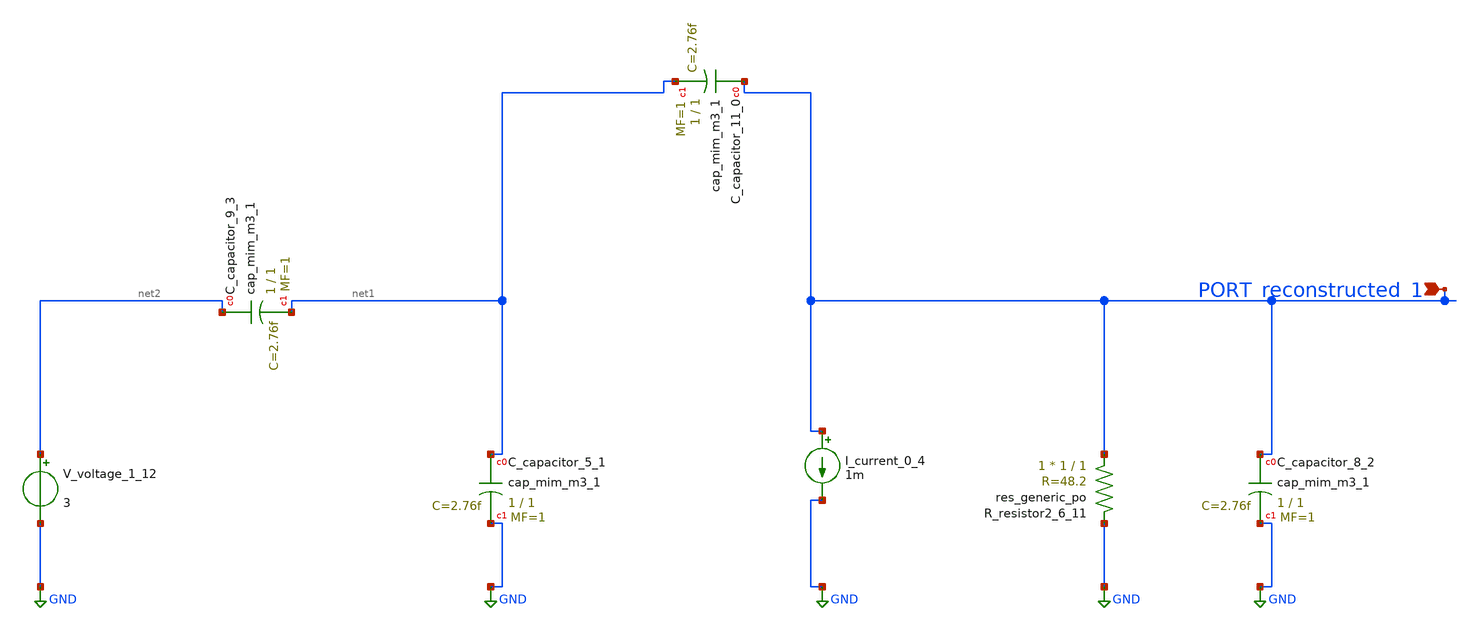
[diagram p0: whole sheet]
** sch_path: schematics/AMSNet/790.sch
**.subckt 790 PORT_reconstructed_1
*.ipin PORT_reconstructed_1
XC_capacitor_11_0 PORT_reconstructed_1 net1 sky130_fd_pr__cap_mim_m3_1 W=1 L=1 MF=1 m=1
XC_capacitor_5_1 net1 GND sky130_fd_pr__cap_mim_m3_1 W=1 L=1 MF=1 m=1
XC_capacitor_8_2 PORT_reconstructed_1 GND sky130_fd_pr__cap_mim_m3_1 W=1 L=1 MF=1 m=1
XC_capacitor_9_3 net2 net1 sky130_fd_pr__cap_mim_m3_1 W=1 L=1 MF=1 m=1
I_current_0_4 PORT_reconstructed_1 GND 1m
XR_resistor2_6_11 PORT_reconstructed_1 GND sky130_fd_pr__res_generic_po W=1 L=1 m=1
V_voltage_1_12 net2 GND 3
**.ends
.GLOBAL GND
.end
